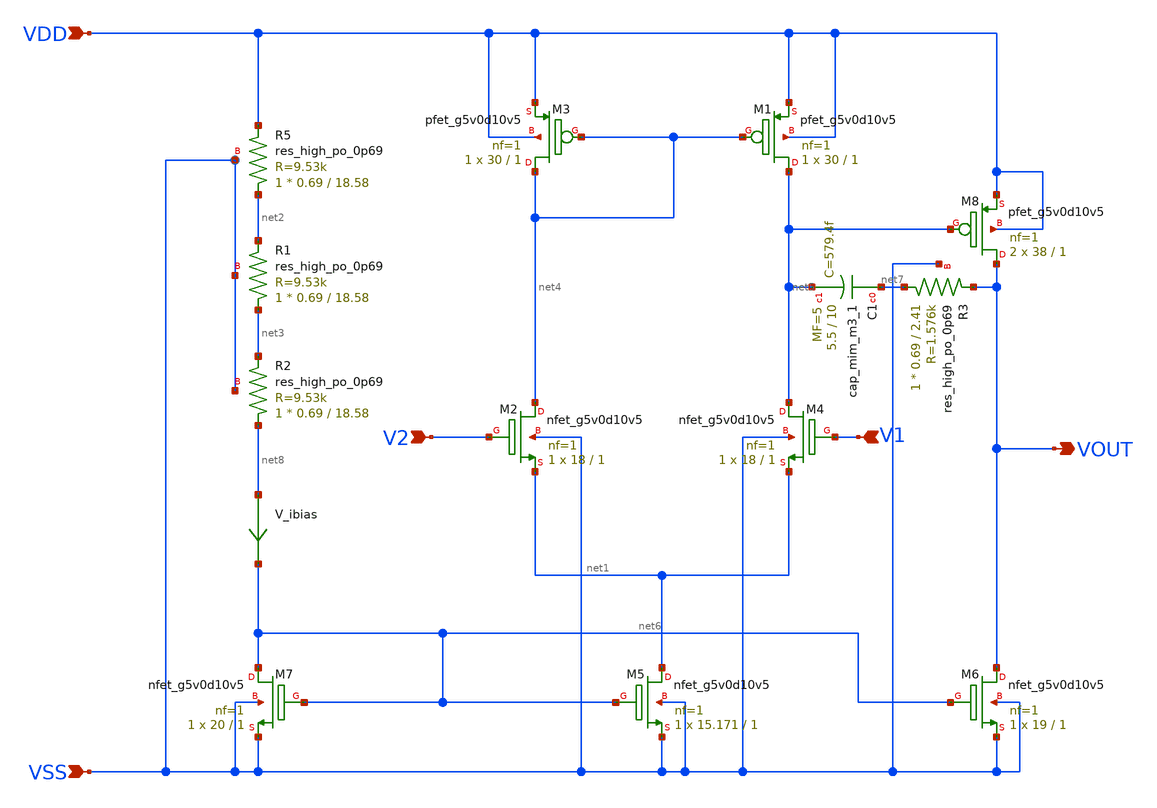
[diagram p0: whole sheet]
** sch_path: xschem/opamp_backup.sch
**.subckt opamp_backup VSS VDD V2 V1 VOUT
*.ipin VSS
*.ipin VDD
*.ipin V2
*.ipin V1
*.opin VOUT
XM2 net4 V2 net1 VSS sky130_fd_pr__nfet_g5v0d10v5 L=1 W=18 nf=1 ad='int((nf+1)/2) * W/nf * 0.29' as='int((nf+2)/2) * W/nf * 0.29'
+ pd='2*int((nf+1)/2) * (W/nf + 0.29)' ps='2*int((nf+2)/2) * (W/nf + 0.29)' nrd='0.29 / W' nrs='0.29 / W'
+ sa=0 sb=0 sd=0 mult=1 m=1
XM1 net5 net4 VDD VDD sky130_fd_pr__pfet_g5v0d10v5 L=1 W=30 nf=1 ad='int((nf+1)/2) * W/nf * 0.29' as='int((nf+2)/2) * W/nf * 0.29'
+ pd='2*int((nf+1)/2) * (W/nf + 0.29)' ps='2*int((nf+2)/2) * (W/nf + 0.29)' nrd='0.29 / W' nrs='0.29 / W'
+ sa=0 sb=0 sd=0 mult=1 m=1
XM4 net5 V1 net1 VSS sky130_fd_pr__nfet_g5v0d10v5 L=1 W=18 nf=1 ad='int((nf+1)/2) * W/nf * 0.29' as='int((nf+2)/2) * W/nf * 0.29'
+ pd='2*int((nf+1)/2) * (W/nf + 0.29)' ps='2*int((nf+2)/2) * (W/nf + 0.29)' nrd='0.29 / W' nrs='0.29 / W'
+ sa=0 sb=0 sd=0 mult=1 m=1
XM5 net1 net6 VSS VSS sky130_fd_pr__nfet_g5v0d10v5 L=1 W=15.171 nf=1 ad='int((nf+1)/2) * W/nf * 0.29'
+ as='int((nf+2)/2) * W/nf * 0.29' pd='2*int((nf+1)/2) * (W/nf + 0.29)' ps='2*int((nf+2)/2) * (W/nf + 0.29)'
+ nrd='0.29 / W' nrs='0.29 / W' sa=0 sb=0 sd=0 mult=1 m=1
XM6 VOUT net6 VSS VSS sky130_fd_pr__nfet_g5v0d10v5 L=1 W=19 nf=1 ad='int((nf+1)/2) * W/nf * 0.29' as='int((nf+2)/2) * W/nf * 0.29'
+ pd='2*int((nf+1)/2) * (W/nf + 0.29)' ps='2*int((nf+2)/2) * (W/nf + 0.29)' nrd='0.29 / W' nrs='0.29 / W'
+ sa=0 sb=0 sd=0 mult=1 m=1
XM7 net6 net6 VSS VSS sky130_fd_pr__nfet_g5v0d10v5 L=1 W=20 nf=1 ad='int((nf+1)/2) * W/nf * 0.29' as='int((nf+2)/2) * W/nf * 0.29'
+ pd='2*int((nf+1)/2) * (W/nf + 0.29)' ps='2*int((nf+2)/2) * (W/nf + 0.29)' nrd='0.29 / W' nrs='0.29 / W'
+ sa=0 sb=0 sd=0 mult=1 m=1
XM3 net4 net4 VDD VDD sky130_fd_pr__pfet_g5v0d10v5 L=1 W=30 nf=1 ad='int((nf+1)/2) * W/nf * 0.29' as='int((nf+2)/2) * W/nf * 0.29'
+ pd='2*int((nf+1)/2) * (W/nf + 0.29)' ps='2*int((nf+2)/2) * (W/nf + 0.29)' nrd='0.29 / W' nrs='0.29 / W'
+ sa=0 sb=0 sd=0 mult=1 m=1
XM8 VOUT net5 VDD VDD sky130_fd_pr__pfet_g5v0d10v5 L=1 W=38 nf=1 ad='int((nf+1)/2) * W/nf * 0.29' as='int((nf+2)/2) * W/nf * 0.29'
+ pd='2*int((nf+1)/2) * (W/nf + 0.29)' ps='2*int((nf+2)/2) * (W/nf + 0.29)' nrd='0.29 / W' nrs='0.29 / W'
+ sa=0 sb=0 sd=0 mult=2 m=2
XC1 net7 net5 sky130_fd_pr__cap_mim_m3_1 W=5.5 L=10 MF=5 m=5
V_ibias net8 net6 0
.save i(v_ibias)
XR5 net2 VDD VSS sky130_fd_pr__res_high_po_0p69 L=18.58 mult=1 m=1
XR1 net3 net2 VSS sky130_fd_pr__res_high_po_0p69 L=18.58 mult=1 m=1
XR2 net8 net3 VSS sky130_fd_pr__res_high_po_0p69 L=18.58 mult=1 m=1
XR3 net7 VOUT VSS sky130_fd_pr__res_high_po_0p69 L=2.41 mult=1 m=1
**.ends
.end
